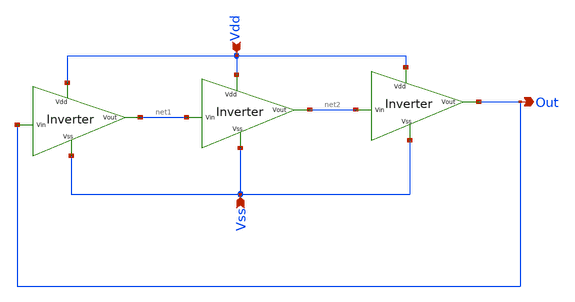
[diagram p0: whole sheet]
** sch_path: Xschem/Ring_Osc_3.sch
**.subckt Ring_Osc_3 Out Vss Vdd
*.opin Out
*.ipin Vss
*.ipin Vdd
x1 Vdd Out net1 Vss inv
x2 Vdd net1 net2 Vss inv
x3 Vdd net2 Out Vss inv
**.ends

* expanding   symbol:  inv.sym # of pins=4
** sym_path: Xschem/inv.sym
** sch_path: Xschem/inv.sch
.subckt inv Vdd Vin Vout Vss
*.ipin Vin
*.ipin Vss
*.ipin Vdd
*.opin Vout
XM1 Vout Vin Vss GND sky130_fd_pr__nfet_01v8 L=0.15 W=1 nf=1 ad='int((nf+1)/2) * W/nf * 0.29' as='int((nf+2)/2) * W/nf * 0.29'
+ pd='2*int((nf+1)/2) * (W/nf + 0.29)' ps='2*int((nf+2)/2) * (W/nf + 0.29)' nrd='0.29 / W' nrs='0.29 / W'
+ sa=0 sb=0 sd=0 mult=1 m=1
XM2 Vout Vin Vdd VDD sky130_fd_pr__pfet_01v8 L=0.15 W=2.5 nf=1 ad='int((nf+1)/2) * W/nf * 0.29' as='int((nf+2)/2) * W/nf * 0.29'
+ pd='2*int((nf+1)/2) * (W/nf + 0.29)' ps='2*int((nf+2)/2) * (W/nf + 0.29)' nrd='0.29 / W' nrs='0.29 / W'
+ sa=0 sb=0 sd=0 mult=1 m=1
.ends

.end
